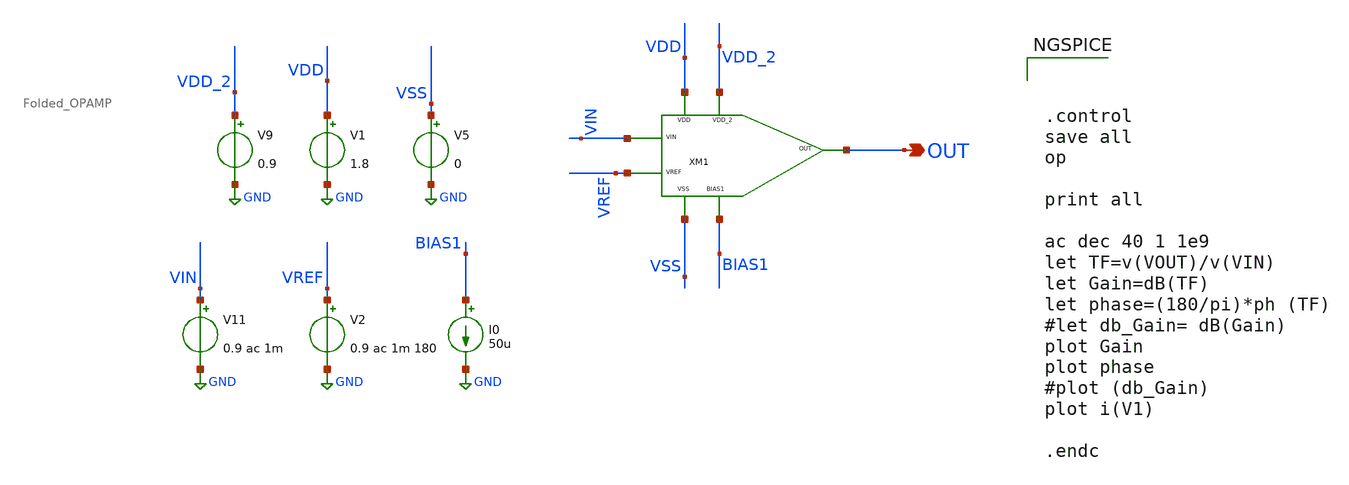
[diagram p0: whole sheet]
** sch_path: xschem/DC_DC_Converter_xschem/OTHERS/DC_DC_Converter_2/DC_DC_Converter/Folded_OPAMP/tb_Folded_OPAMP.sch
**.subckt tb_Folded_OPAMP OUT
*.opin OUT
I0 BIAS1 GND 50u
V9 VDD_2 GND 0.9
V1 VDD GND 1.8
V5 VSS GND 0
V11 VIN GND 0.9 ac 1m
V2 VREF GND 0.9 ac 1m 180
XM1 VDD VSS VDD_2 BIAS1 OUT VIN VREF Folded_OPAMP
**** begin user architecture code

** opencircuitdesign pdks install
.lib $::SKYWATER_MODELS/sky130.lib.spice tt





.control
save all
op

print all

ac dec 40 1 1e9
let TF=v(VOUT)/v(VIN)
let Gain=dB(TF)
let phase=(180/pi)*ph (TF)
#let db_Gain= dB(Gain)
plot Gain
plot phase
#plot (db_Gain)
plot i(V1)

.endc


**** end user architecture code
**.ends
.GLOBAL GND
.end
